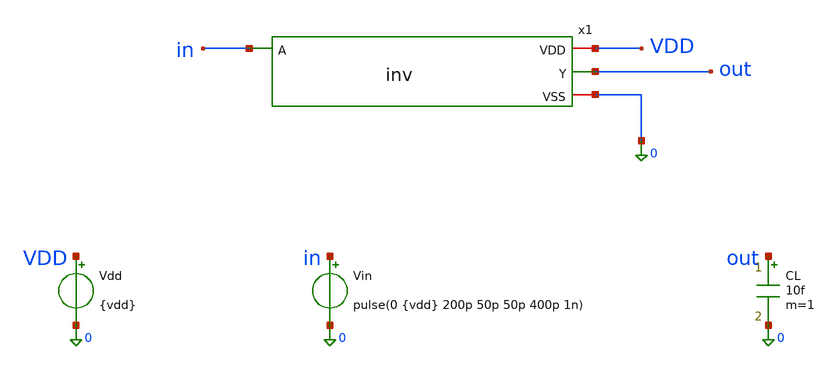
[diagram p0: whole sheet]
** sch_path: cdept-gui/tutorials/start/inv-tb/libs/work/tb_inv/schematic/tb_inv.sch
**.subckt tb_inv
x1 VDD in out 0 inv
Vdd VDD 0 {vdd}
Vin in 0 pulse(0 {vdd} 200p 50p 50p 400p 1n)
CL out 0 10f m=1
**.ends
.end
